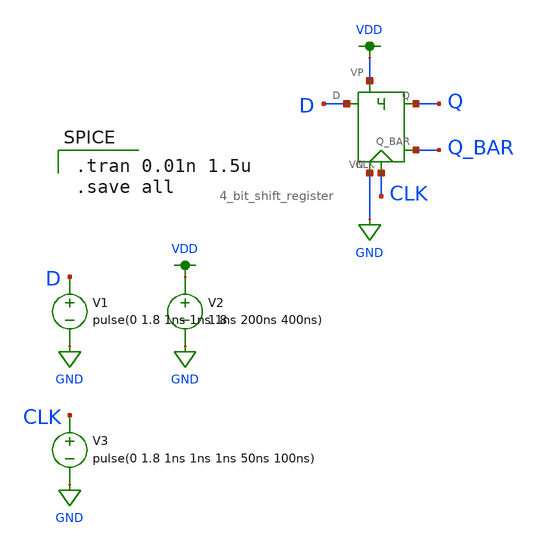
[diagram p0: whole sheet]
** sch_path: mp2/schematics/crsl_d_flip_flop_tran.sch
**.subckt crsl_d_flip_flop_tran
V1 D GND pulse(0 1.8 1ns 1ns 1ns 200ns 400ns)
V2 VDD GND 1.8
V3 CLK GND pulse(0 1.8 1ns 1ns 1ns 50ns 100ns)
X1 D Q_BAR VDD Q CLK GND 4_bit_shift_register
**** begin user architecture code

.option wnflag=1
.lib ~/skywater/skywater-pdk/libraries/sky130_fd_pr_ngspice/latest/models/sky130.lib.spice tt


.tran 0.01n 1.5u
.save all

**** end user architecture code
**.ends
.GLOBAL GND
.GLOBAL VDD
.end
